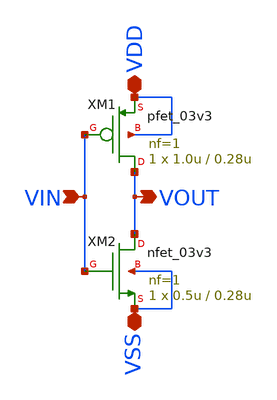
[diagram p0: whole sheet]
** sch_path: sar_logic/sar_designs/inv_OLD.sch
**.subckt inv_OLD VIN VOUT VSS VDD
*.ipin VIN
*.opin VOUT
*.iopin VSS
*.iopin VDD
XM1 VOUT VIN VDD VDD pfet_03v3 L=0.28u W=1.0u nf=1 ad='int((nf+1)/2) * W/nf * 0.18u' as='int((nf+2)/2) * W/nf * 0.18u'
+ pd='2*int((nf+1)/2) * (W/nf + 0.18u)' ps='2*int((nf+2)/2) * (W/nf + 0.18u)' nrd='0.18u / W' nrs='0.18u / W'
+ sa=0 sb=0 sd=0 m=1
XM2 VOUT VIN VSS VSS nfet_03v3 L=0.28u W=0.5u nf=1 ad='int((nf+1)/2) * W/nf * 0.18u' as='int((nf+2)/2) * W/nf * 0.18u'
+ pd='2*int((nf+1)/2) * (W/nf + 0.18u)' ps='2*int((nf+2)/2) * (W/nf + 0.18u)' nrd='0.18u / W' nrs='0.18u / W'
+ sa=0 sb=0 sd=0 m=1
**.ends
.end
